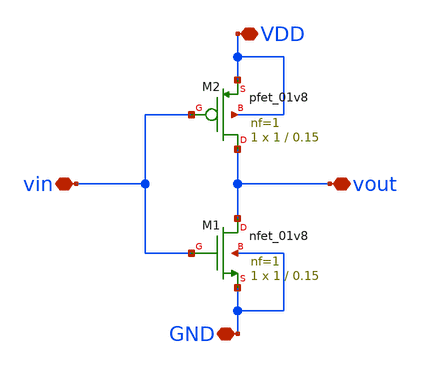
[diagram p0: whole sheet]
** sch_path: SCH/inverter.sch
**.subckt inverter VDD vout vin GND
*.iopin VDD
*.iopin vout
*.iopin vin
*.iopin GND
XM1 vout vin GND GND sky130_fd_pr__nfet_01v8 L=0.15 W=1 nf=1 ad='int((1 + 1)/2) * 1 / 1 * 0.29' as='int((1 + 2)/2) * 1 / 1 * 0.29'
+ pd='2*int((1 + 1)/2) * (1 / 1 + 0.29)' ps='2*int((1 + 2)/2) * (1 / 1 + 0.29)' nrd='0.29 / 1 ' nrs='0.29 / 1 '
+ sa=0 sb=0 sd=0 mult=1 m=1
XM2 vout vin VDD VDD sky130_fd_pr__pfet_01v8 L=0.15 W=1 nf=1 ad='int((1 + 1)/2) * 1 / 1 * 0.29' as='int((1 + 2)/2) * 1 / 1 * 0.29'
+ pd='2*int((1 + 1)/2) * (1 / 1 + 0.29)' ps='2*int((1 + 2)/2) * (1 / 1 + 0.29)' nrd='0.29 / 1 ' nrs='0.29 / 1 '
+ sa=0 sb=0 sd=0 mult=1 m=1
**.ends
.end
